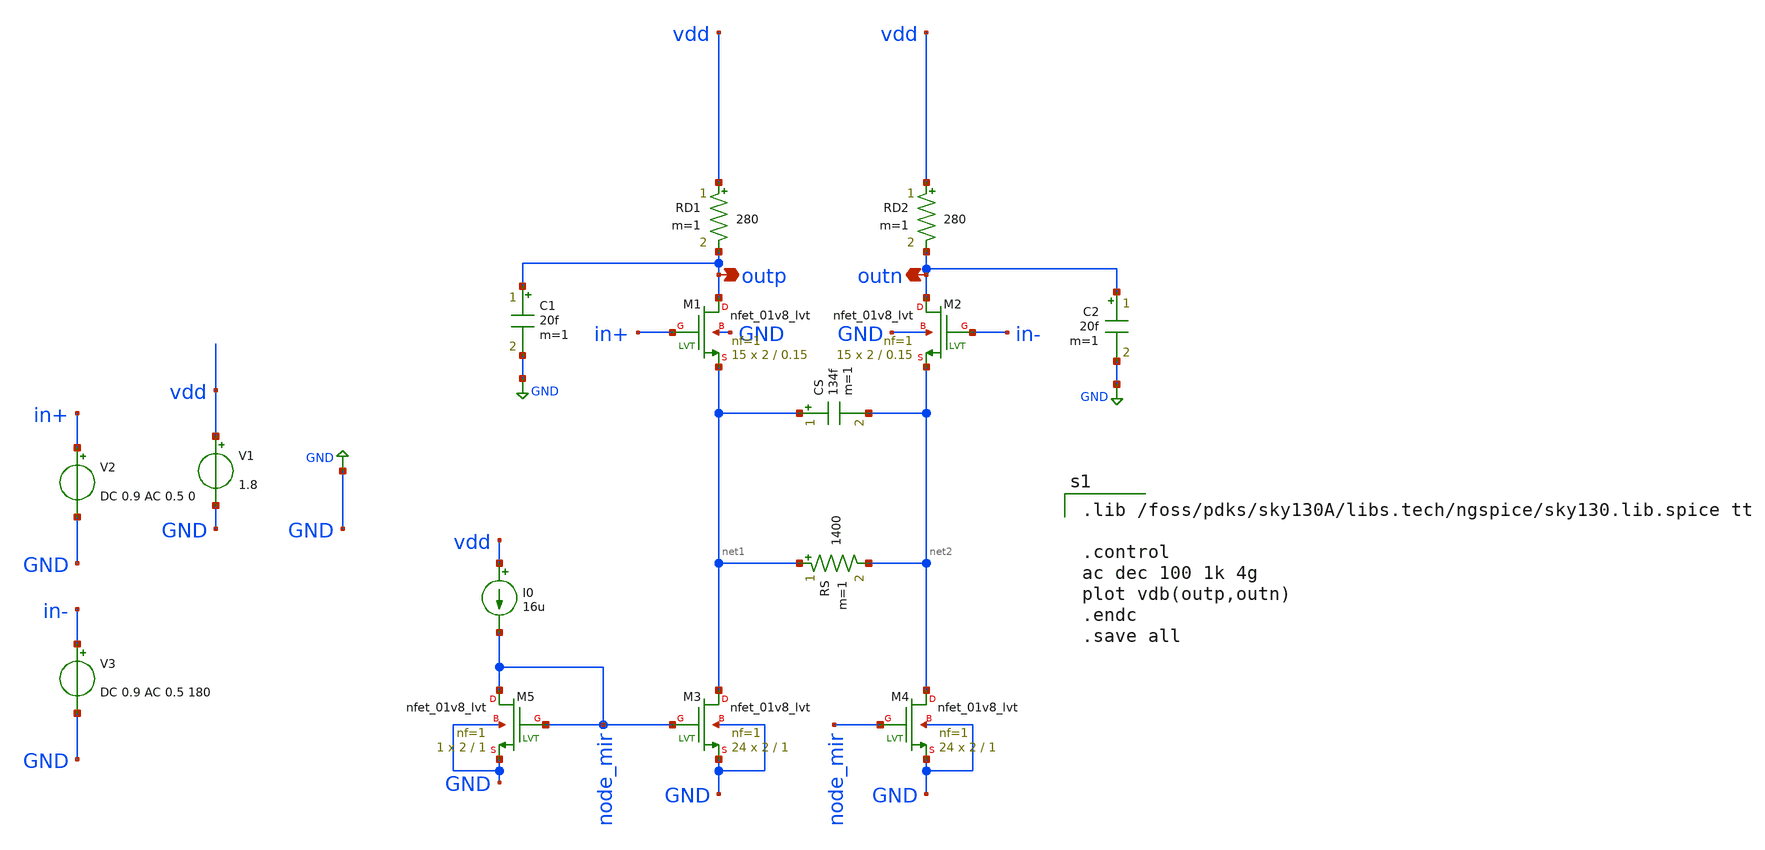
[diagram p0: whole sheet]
** sch_path: CTLE/ctle_low_power.sch
**.subckt ctle_low_power outp outn
*.opin outp
*.opin outn
V1 vdd GND 1.8
V2 in+ GND DC 0.9 AC 0.5 0
V3 in- GND DC 0.9 AC 0.5 180
XM1 outp in+ net1 GND sky130_fd_pr__nfet_01v8_lvt L=0.15 W=2 nf=1 ad='int((nf+1)/2) * W/nf * 0.29' as='int((nf+2)/2) * W/nf * 0.29'
+ pd='2*int((nf+1)/2) * (W/nf + 0.29)' ps='2*int((nf+2)/2) * (W/nf + 0.29)' nrd='0.29 / W' nrs='0.29 / W'
+ sa=0 sb=0 sd=0 mult=15 m=15
XM2 outn in- net2 GND sky130_fd_pr__nfet_01v8_lvt L=0.15 W=2 nf=1 ad='int((nf+1)/2) * W/nf * 0.29' as='int((nf+2)/2) * W/nf * 0.29'
+ pd='2*int((nf+1)/2) * (W/nf + 0.29)' ps='2*int((nf+2)/2) * (W/nf + 0.29)' nrd='0.29 / W' nrs='0.29 / W'
+ sa=0 sb=0 sd=0 mult=15 m=15
I0 vdd node_mir 16u
XM3 net1 node_mir GND GND sky130_fd_pr__nfet_01v8_lvt L=1 W=2 nf=1 ad='int((nf+1)/2) * W/nf * 0.29' as='int((nf+2)/2) * W/nf * 0.29'
+ pd='2*int((nf+1)/2) * (W/nf + 0.29)' ps='2*int((nf+2)/2) * (W/nf + 0.29)' nrd='0.29 / W' nrs='0.29 / W'
+ sa=0 sb=0 sd=0 mult=24 m=24
XM4 net2 node_mir GND GND sky130_fd_pr__nfet_01v8_lvt L=1 W=2 nf=1 ad='int((nf+1)/2) * W/nf * 0.29' as='int((nf+2)/2) * W/nf * 0.29'
+ pd='2*int((nf+1)/2) * (W/nf + 0.29)' ps='2*int((nf+2)/2) * (W/nf + 0.29)' nrd='0.29 / W' nrs='0.29 / W'
+ sa=0 sb=0 sd=0 mult=24 m=24
XM5 node_mir node_mir GND GND sky130_fd_pr__nfet_01v8_lvt L=1 W=2 nf=1 ad='int((nf+1)/2) * W/nf * 0.29'
+ as='int((nf+2)/2) * W/nf * 0.29' pd='2*int((nf+1)/2) * (W/nf + 0.29)' ps='2*int((nf+2)/2) * (W/nf + 0.29)'
+ nrd='0.29 / W' nrs='0.29 / W' sa=0 sb=0 sd=0 mult=1 m=1
RD1 vdd outp 280 m=1
RD2 vdd outn 280 m=1
CS net1 net2 134f m=1
RS net1 net2 1400 m=1
C1 outp GND 20f m=1
C2 outn GND 20f m=1
**** begin user architecture code

.lib /foss/pdks/sky130A/libs.tech/ngspice/sky130.lib.spice tt

.control
ac dec 100 1k 4g
plot vdb(outp,outn)
.endc
.save all


**** end user architecture code
**.ends
.GLOBAL GND
.end
